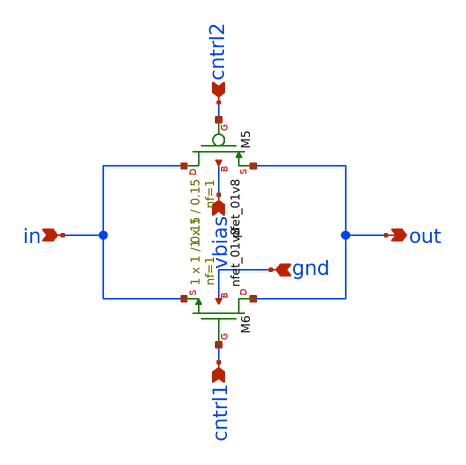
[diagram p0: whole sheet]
** sch_path: xschem/attenuator/gate-switch.sch
**.subckt gate-switch in vbias gnd out cntrl1 cntrl2
*.ipin in
*.ipin vbias
*.ipin gnd
*.opin out
*.ipin cntrl1
*.ipin cntrl2
XM5 in cntrl2 out vbias sky130_fd_pr__pfet_01v8 L=0.15 W=1 nf=1 ad='int((nf+1)/2) * W/nf * 0.29' as='int((nf+2)/2) * W/nf * 0.29'
+ pd='2*int((nf+1)/2) * (W/nf + 0.29)' ps='2*int((nf+2)/2) * (W/nf + 0.29)' nrd='0.29 / W' nrs='0.29 / W'
+ sa=0 sb=0 sd=0 mult=1 m=1
XM6 out cntrl1 in gnd sky130_fd_pr__nfet_01v8 L=0.15 W=1 nf=1 ad='int((nf+1)/2) * W/nf * 0.29' as='int((nf+2)/2) * W/nf * 0.29'
+ pd='2*int((nf+1)/2) * (W/nf + 0.29)' ps='2*int((nf+2)/2) * (W/nf + 0.29)' nrd='0.29 / W' nrs='0.29 / W'
+ sa=0 sb=0 sd=0 mult=1 m=1
**** begin user architecture code
 ** manual skywater pdks install (with patches applied)
* .lib $::SKYWATER_MODELS/models/sky130.lib.spice tt
*** remove the /models/

** opencircuitdesign pdks install
.lib /Volumes/WORK_DRIVE/open_pdks/sky130/custom/models/sky130.lib.spice tt

.param mc_mm_switch=0
.param mc_pr_switch=0

**** end user architecture code
**.ends
.end
